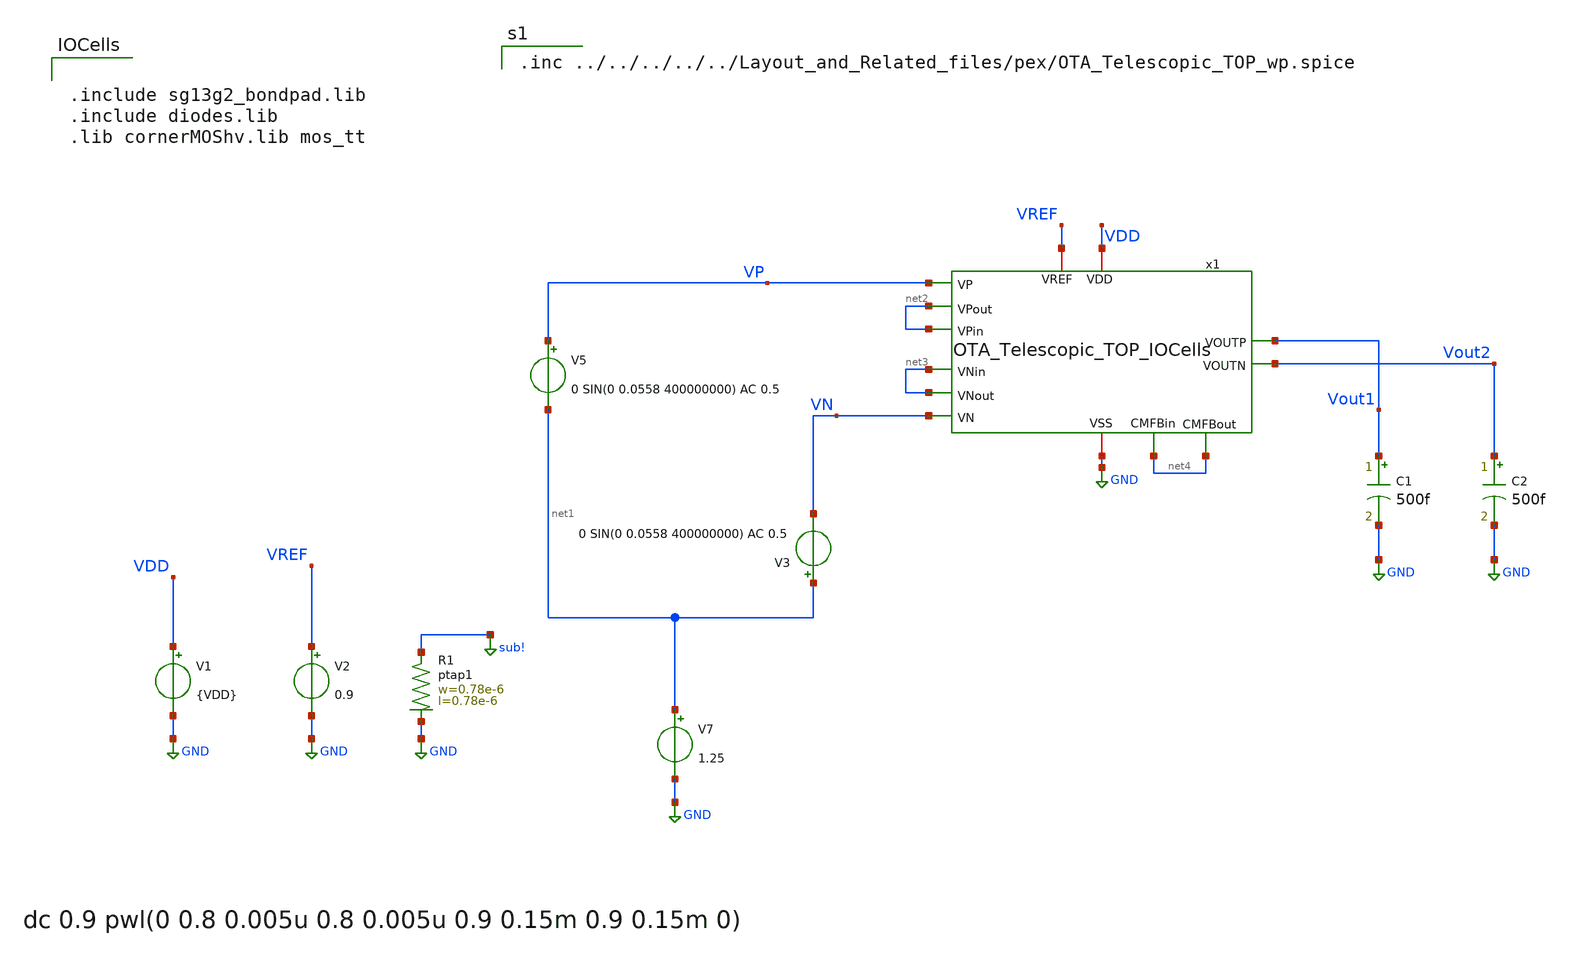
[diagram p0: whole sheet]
** sch_path: OTA_Telescopic/AutoTestbench/tb/done/OTA_Telescopic_TOP_TB_CL_AC_io.sch
**.subckt OTA_Telescopic_TOP_TB_CL_AC_io
V7 net1 GND 1.25
V5 VP net1 0 SIN(0 0.0558 400000000) AC 0.5
V1 VDD GND {VDD}
V2 VREF GND 0.9
C1 Vout1 GND 500f m=1
C2 Vout2 GND 500f m=1
V3 net1 VN 0 SIN(0 0.0558 400000000) AC 0.5
x1 VDD GND net2 VP net2 Vout2 Vout1 net3 net3 VN VREF net4 net4 OTA_Telescopic_TOP_IOCells
XR1 sub! GND ptap1 R=262.8 w=0.78e-6 l=0.78e-6
**** begin user architecture code


** opencircuitdesign pdks install
.lib cornerMOSlv.lib mos_$PROCESS
.lib cornerRES.lib res_typ
.lib cornerCAP.lib cap_typ
.temp $TEMP





.nodeset v(Vout1)=0.9 v(Vout2)=0.9
.param VDD=$VDD
.control
save Vout1 Vout2

* AC simulation
ac dec 1k 1 1T
let Av = db(v(Vout1)-v(Vout2))
meas ac Ao FIND Av WHEN frequency=10
let ABW = Ao-3
meas ac BW WHEN Av=ABW
meas ac UGBW WHEN Av=0
let phase_vec = 180/pi*cph(v(Vout1)-v(Vout2))

* Phase margin (PM)
meas ac phase FIND phase_vec WHEN frequency=UGBW
let PM = phase+180
print PM

* Gain margin (GM)
meas ac freq180 FIND frequency WHEN phase_vec=-180
meas ac gain FIND Av WHEN frequency=freq180
let GM = 0-gain

print GM
plot Av
plot phase_vec

write AC_OL.raw
wrdata AvCL.txt Av

let Ao_ = Ao
let BW_ = BW

echo Ao $&Ao_ >> results.txt
echo BW $&BW_ >> results.txt

.endc




.include sg13g2_bondpad.lib
.include diodes.lib
.lib cornerMOShv.lib mos_tt



.inc ../../../../../Layout_and_Related_files/pex/OTA_Telescopic_TOP_wp.spice

**** end user architecture code
**.ends
.GLOBAL GND
.GLOBAL sub!
.end
